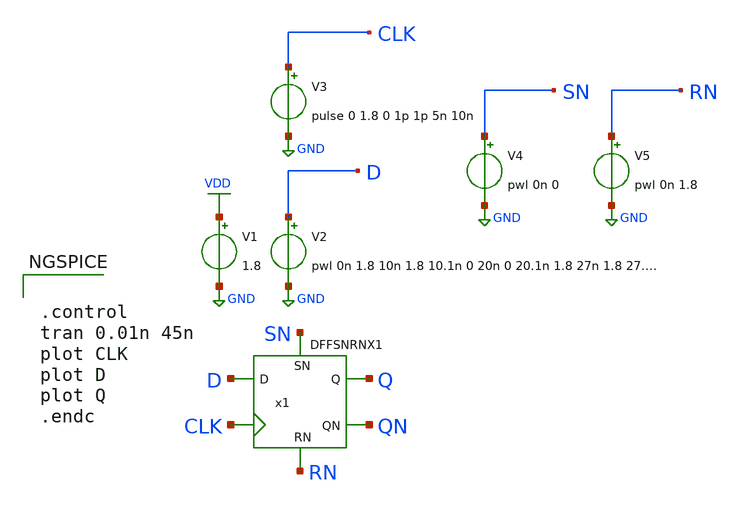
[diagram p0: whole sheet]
** sch_path: lib/xschem/test_DFFSNRNX1.sch
**.subckt test_DFFSNRNX1
V2 D GND pwl 0n 1.8 10n 1.8 10.1n 0 20n 0 20.1n 1.8 27n 1.8 27.1n 0 34n 0 34.1n 1.8
V1 VDD GND 1.8
V3 CLK GND pulse 0 1.8 0 1p 1p 5n 10n
V4 SN GND pwl 0n 0
V5 RN GND pwl 0n 1.8
x1 Q QN D CLK SN RN VDD GND DFFSNRNX1
**** begin user architecture code

.lib $::SKYWATER_MODELS/sky130.lib.spice tt


**** end user architecture code
**.ends

* expanding   symbol:  DFFSNRNX1.sym # of pins=6
** sym_path: DFFSNRNX1.sym
** sch_path: DFFSNRNX1.sch
.subckt DFFSNRNX1 Q QN D CLK SN RN VDD VSS
*.ipin D
*.opin QN
*.ipin SN
*.ipin CLK
*.opin Q
*.ipin RN
x1 net3 net1 SN net4 VDD VSS NAND3X1
x3 net2 net1 CLK net4 VDD VSS NAND3X1
x6 Q QN SN net4 VDD VSS NAND3X1
x2 net1 D RN net2 VDD VSS NAND3X1
x4 net4 net3 CLK RN VDD VSS NAND3X1
x5 QN net2 RN Q VDD VSS NAND3X1
.ends


* expanding   symbol:  NAND3X1.sym # of pins=4
** sym_path: lib/xschem/NAND3X1.sym
** sch_path: lib/xschem/NAND3X1.sch
.subckt NAND3X1 Y A B C VDD VSS
*.ipin A
*.opin Y
*.ipin B
*.ipin C
XM1 net2 C VSS VSS sky130_fd_pr__nfet_01v8 L=0.15 W=3 nf=1 ad='int((nf+1)/2) * W/nf * 0.29' as='int((nf+2)/2) * W/nf * 0.29'
+ pd='2*int((nf+1)/2) * (W/nf + 0.29)' ps='2*int((nf+2)/2) * (W/nf + 0.29)' nrd='0.29 / W' nrs='0.29 / W'
+ sa=0 sb=0 sd=0 mult=1 m=1
XM2 Y A VDD VDD sky130_fd_pr__pfet_01v8 L=0.15 W=2 nf=1 ad='int((nf+1)/2) * W/nf * 0.29' as='int((nf+2)/2) * W/nf * 0.29'
+ pd='2*int((nf+1)/2) * (W/nf + 0.29)' ps='2*int((nf+2)/2) * (W/nf + 0.29)' nrd='0.29 / W' nrs='0.29 / W'
+ sa=0 sb=0 sd=0 mult=1 m=1
XM3 net1 B net2 VSS sky130_fd_pr__nfet_01v8 L=0.15 W=3 nf=1 ad='int((nf+1)/2) * W/nf * 0.29' as='int((nf+2)/2) * W/nf * 0.29'
+ pd='2*int((nf+1)/2) * (W/nf + 0.29)' ps='2*int((nf+2)/2) * (W/nf + 0.29)' nrd='0.29 / W' nrs='0.29 / W'
+ sa=0 sb=0 sd=0 mult=1 m=1
XM4 Y A net1 VSS sky130_fd_pr__nfet_01v8 L=0.15 W=3 nf=1 ad='int((nf+1)/2) * W/nf * 0.29' as='int((nf+2)/2) * W/nf * 0.29'
+ pd='2*int((nf+1)/2) * (W/nf + 0.29)' ps='2*int((nf+2)/2) * (W/nf + 0.29)' nrd='0.29 / W' nrs='0.29 / W'
+ sa=0 sb=0 sd=0 mult=1 m=1
XM5 Y A VDD VDD sky130_fd_pr__pfet_01v8 L=0.15 W=2 nf=1 ad='int((nf+1)/2) * W/nf * 0.29' as='int((nf+2)/2) * W/nf * 0.29'
+ pd='2*int((nf+1)/2) * (W/nf + 0.29)' ps='2*int((nf+2)/2) * (W/nf + 0.29)' nrd='0.29 / W' nrs='0.29 / W'
+ sa=0 sb=0 sd=0 mult=1 m=1
XM6 Y B VDD VDD sky130_fd_pr__pfet_01v8 L=0.15 W=2 nf=1 ad='int((nf+1)/2) * W/nf * 0.29' as='int((nf+2)/2) * W/nf * 0.29'
+ pd='2*int((nf+1)/2) * (W/nf + 0.29)' ps='2*int((nf+2)/2) * (W/nf + 0.29)' nrd='0.29 / W' nrs='0.29 / W'
+ sa=0 sb=0 sd=0 mult=1 m=1
XM7 Y B VDD VDD sky130_fd_pr__pfet_01v8 L=0.15 W=2 nf=1 ad='int((nf+1)/2) * W/nf * 0.29' as='int((nf+2)/2) * W/nf * 0.29'
+ pd='2*int((nf+1)/2) * (W/nf + 0.29)' ps='2*int((nf+2)/2) * (W/nf + 0.29)' nrd='0.29 / W' nrs='0.29 / W'
+ sa=0 sb=0 sd=0 mult=1 m=1
XM8 Y C VDD VDD sky130_fd_pr__pfet_01v8 L=0.15 W=2 nf=1 ad='int((nf+1)/2) * W/nf * 0.29' as='int((nf+2)/2) * W/nf * 0.29'
+ pd='2*int((nf+1)/2) * (W/nf + 0.29)' ps='2*int((nf+2)/2) * (W/nf + 0.29)' nrd='0.29 / W' nrs='0.29 / W'
+ sa=0 sb=0 sd=0 mult=1 m=1
XM9 Y C VDD VDD sky130_fd_pr__pfet_01v8 L=0.15 W=2 nf=1 ad='int((nf+1)/2) * W/nf * 0.29' as='int((nf+2)/2) * W/nf * 0.29'
+ pd='2*int((nf+1)/2) * (W/nf + 0.29)' ps='2*int((nf+2)/2) * (W/nf + 0.29)' nrd='0.29 / W' nrs='0.29 / W'
+ sa=0 sb=0 sd=0 mult=1 m=1
.ends

.GLOBAL VDD
.GLOBAL GND
**** begin user architecture code


.control
tran 0.01n 45n
plot CLK
plot D
plot Q
.endc


**** end user architecture code
.end
